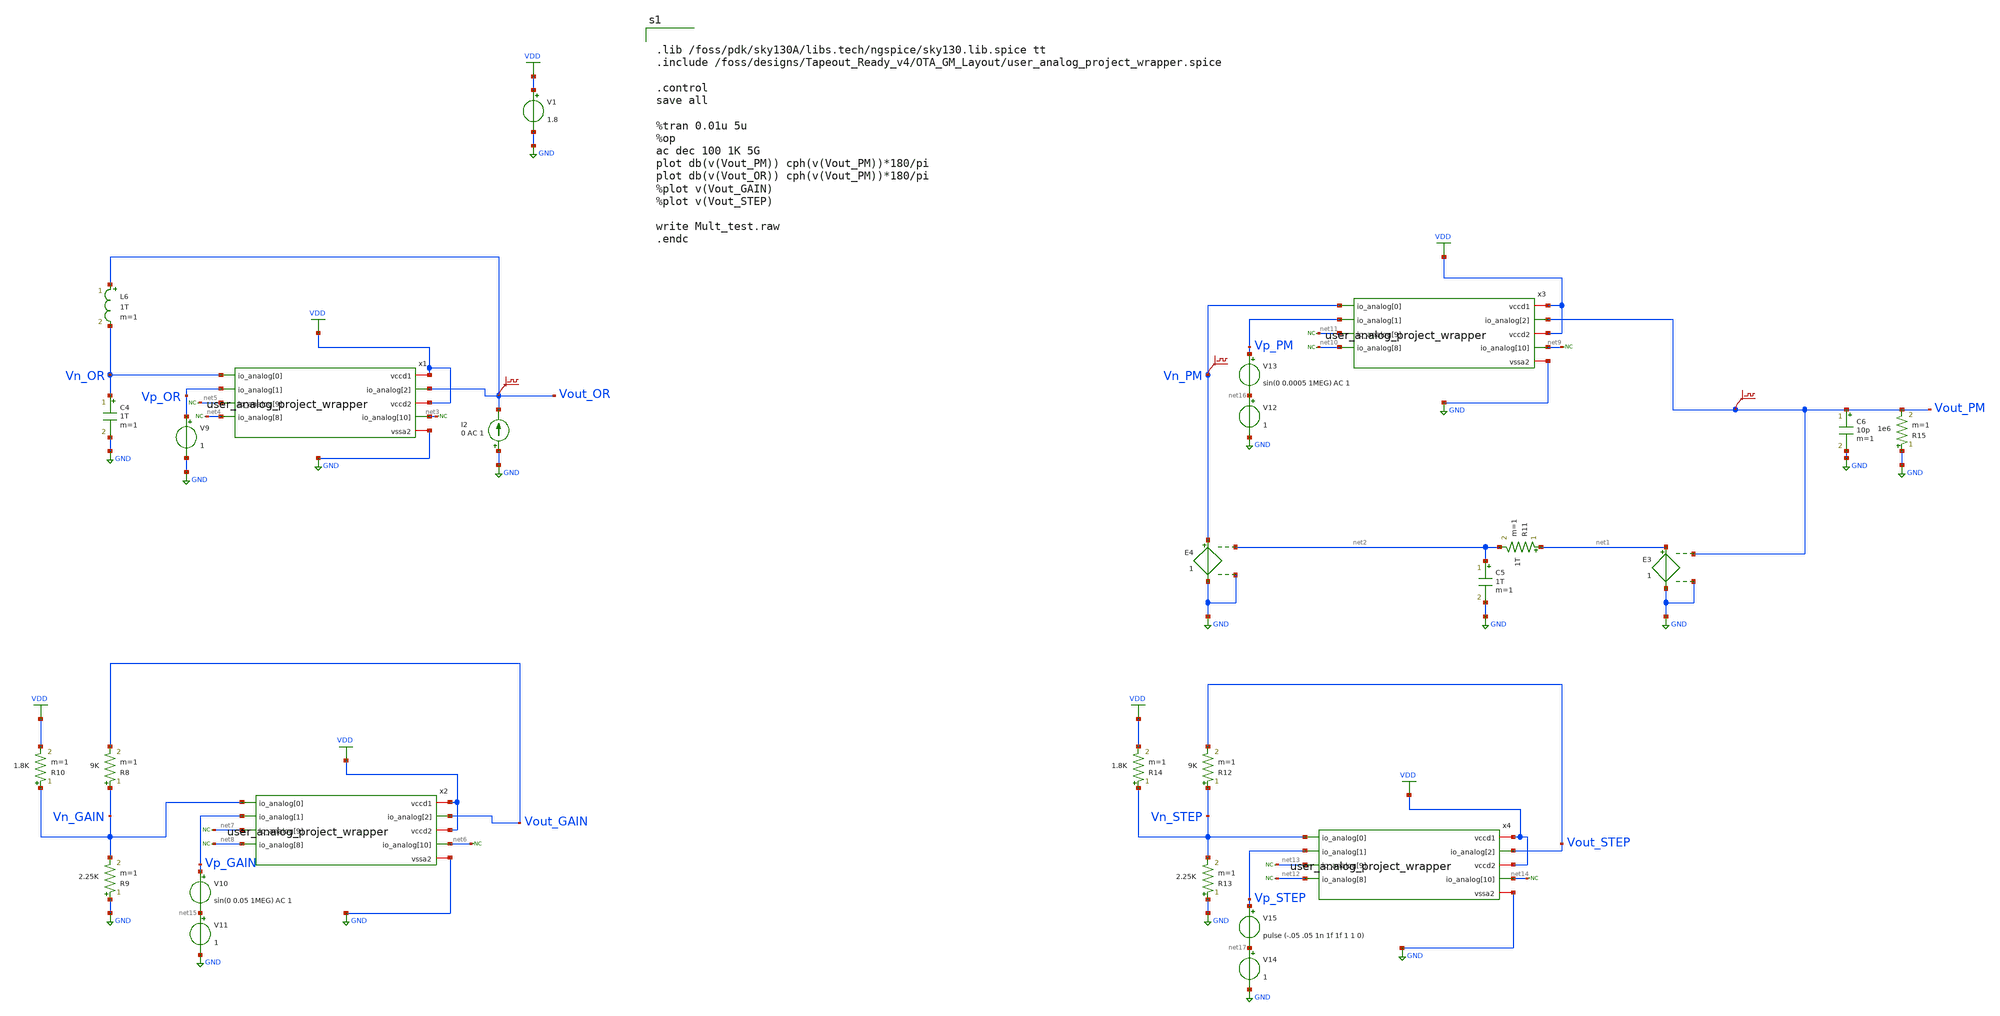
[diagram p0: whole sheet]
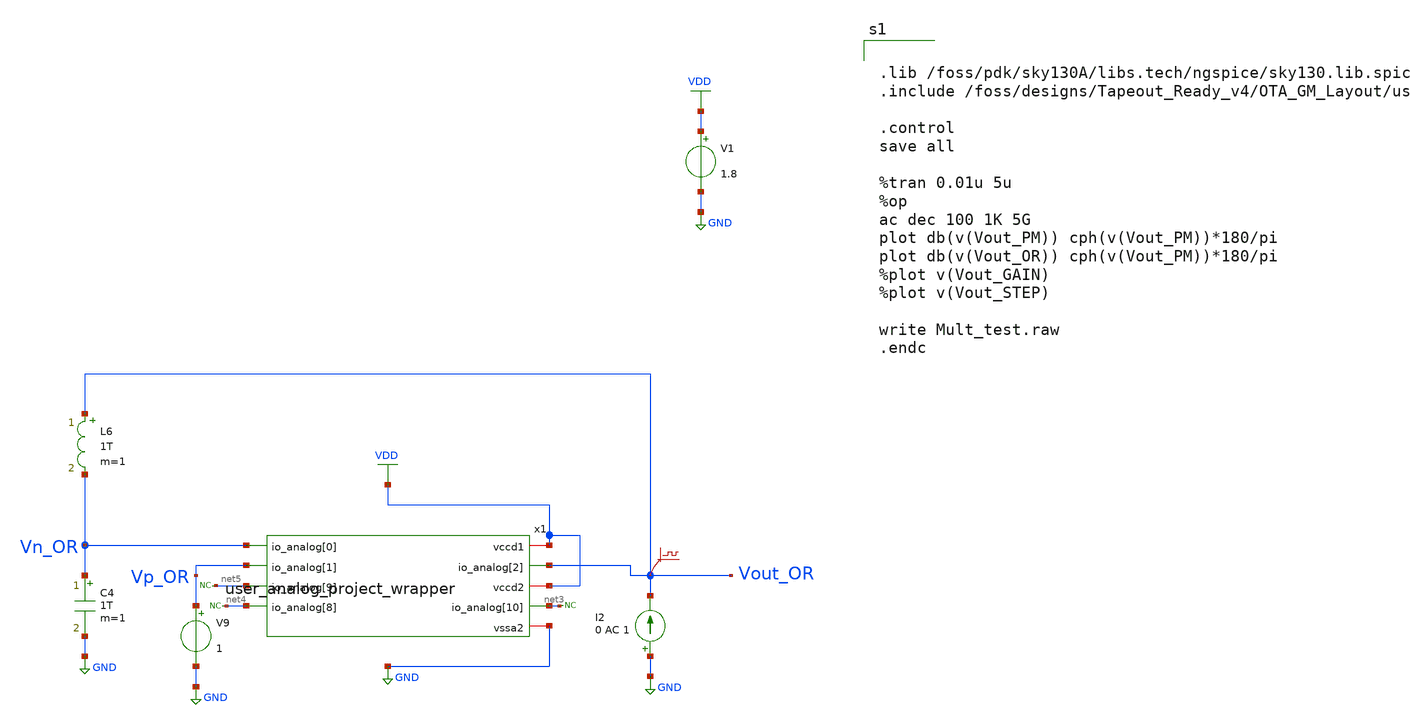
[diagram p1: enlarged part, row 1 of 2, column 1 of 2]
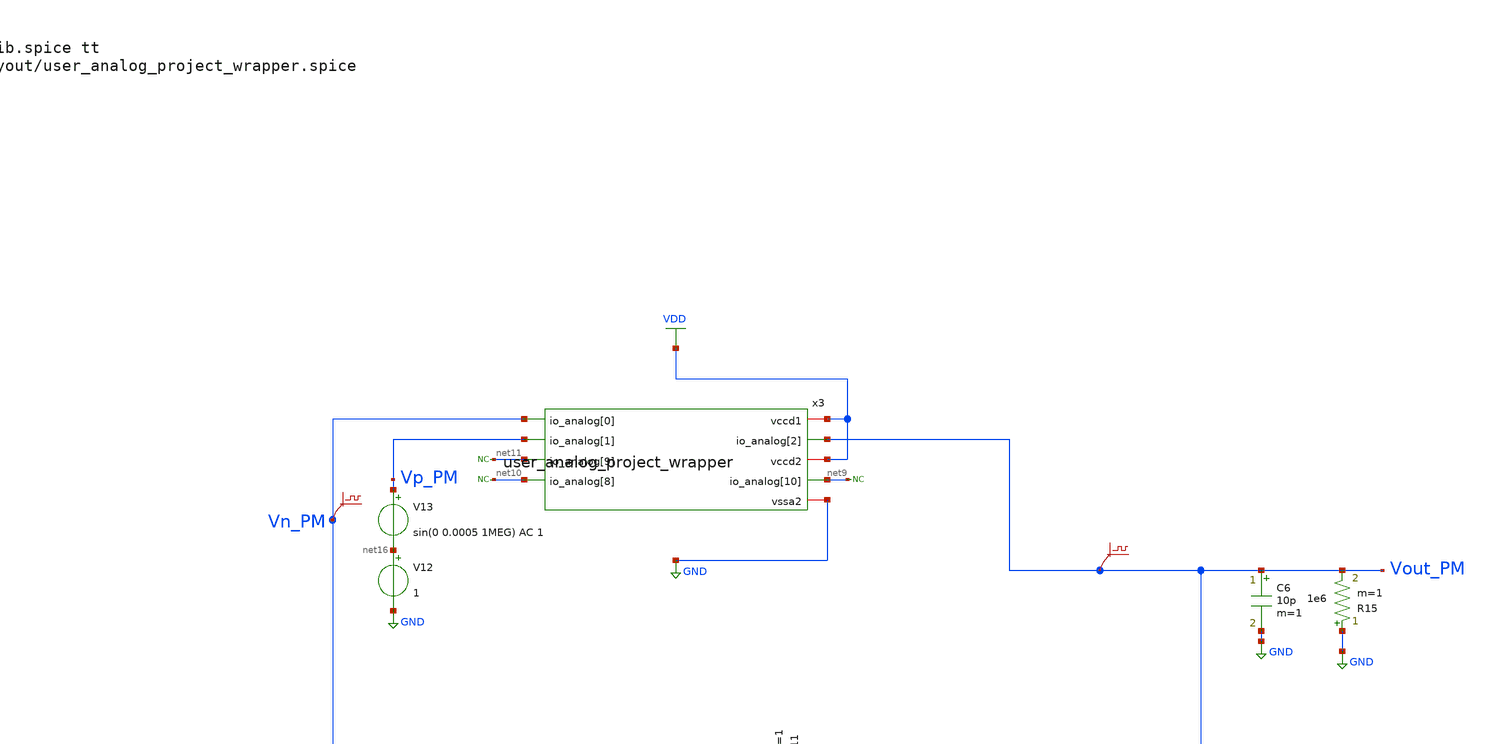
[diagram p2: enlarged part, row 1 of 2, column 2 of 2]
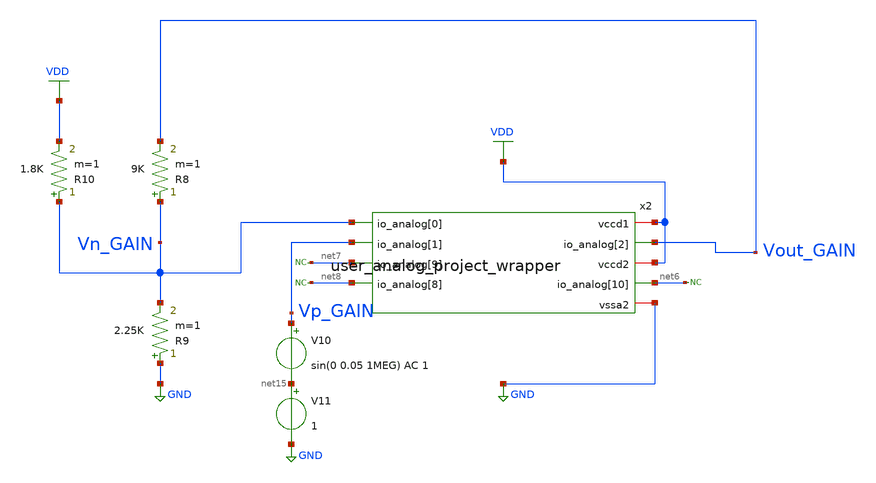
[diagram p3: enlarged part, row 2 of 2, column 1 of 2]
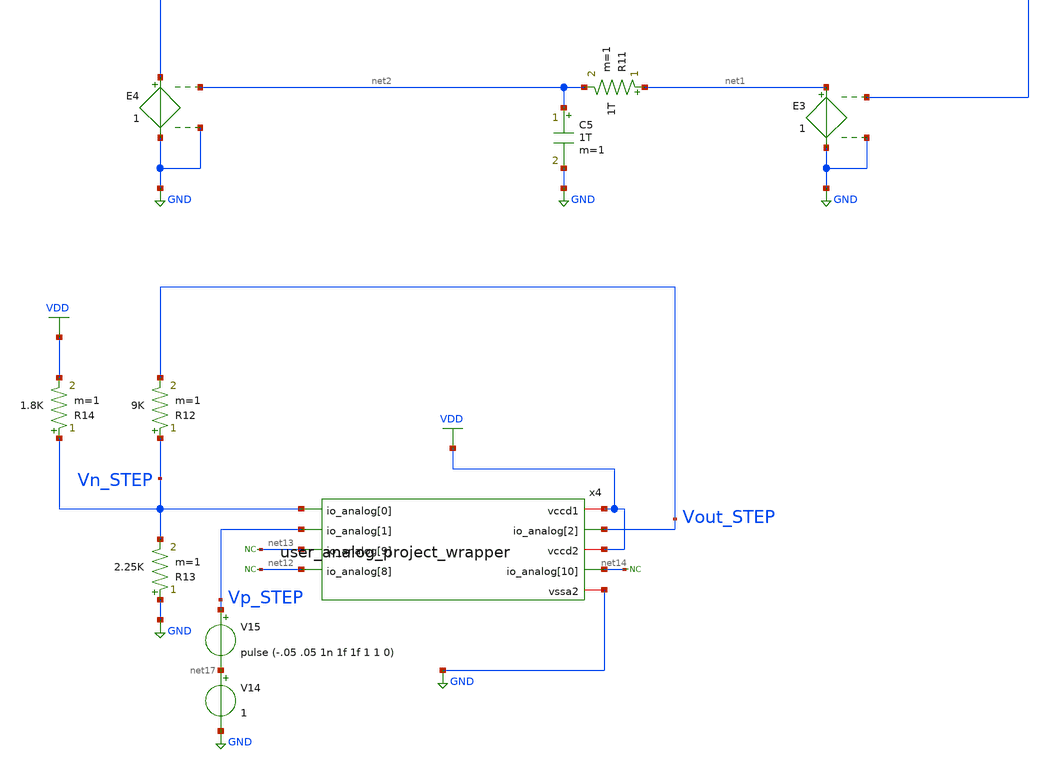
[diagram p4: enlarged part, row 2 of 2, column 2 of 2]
** sch_path: SP23_Tapeout/Tapeout_Ready_v5/OTA_GM_Schematic/Mult_test.sch
**.subckt Mult_test
V9 Vp_OR GND 1
.save v(vout_or)
I2 GND Vout_OR 0 AC 1
L6 Vout_OR Vn_OR 1T m=1
C4 Vn_OR GND 1T m=1
R8 Vn_GAIN Vout_GAIN 9K m=1
R9 GND Vn_GAIN 2.25K m=1
R10 Vn_GAIN VDD 1.8K m=1
V10 Vp_GAIN net15 sin(0 0.05 1MEG) AC 1
V11 net15 GND 1
E3 net1 GND Vout_PM GND 1
E4 Vn_PM GND net2 GND 1
V12 net16 GND 1
.save v(vout_pm)
V13 Vp_PM net16 sin(0 0.0005 1MEG) AC 1
C5 net2 GND 1T m=1
R11 net1 net2 1T m=1
.save v(vn_pm)
R12 Vn_STEP Vout_STEP 9K m=1
R13 GND Vn_STEP 2.25K m=1
R14 Vn_STEP VDD 1.8K m=1
V14 net17 GND 1
V15 Vp_STEP net17 pulse (-.05 .05 1n 1f 1f 1 1 0)
C6 Vout_PM GND 10p m=1
R15 GND Vout_PM 1e6 m=1
* noconn #net9
* noconn #net14
* noconn #net6
* noconn #net5
* noconn #net3
* noconn #net4
* noconn #net7
* noconn #net8
* noconn #net11
* noconn #net10
* noconn #net13
* noconn #net12
V1 VDD GND 1.8
x1 Vn_OR net3 Vp_OR Vout_OR net4 net5 GND VDD VDD user_analog_project_wrapper
x2 Vn_GAIN net6 Vp_GAIN Vout_GAIN net8 net7 GND VDD VDD user_analog_project_wrapper
x3 Vn_PM net9 Vp_PM Vout_PM net10 net11 GND VDD VDD user_analog_project_wrapper
x4 Vn_STEP net14 Vp_STEP Vout_STEP net12 net13 GND VDD VDD user_analog_project_wrapper
**** begin user architecture code


.lib /foss/pdk/sky130A/libs.tech/ngspice/sky130.lib.spice tt
.include /foss/designs/Tapeout_Ready_v4/OTA_GM_Layout/user_analog_project_wrapper.spice

.control
save all

%tran 0.01u 5u
%op
ac dec 100 1K 5G
plot db(v(Vout_PM)) cph(v(Vout_PM))*180/pi
plot db(v(Vout_OR)) cph(v(Vout_PM))*180/pi
%plot v(Vout_GAIN)
%plot v(Vout_STEP)

write Mult_test.raw
.endc


**** end user architecture code
**.ends
.GLOBAL GND
.GLOBAL VDD
.end
